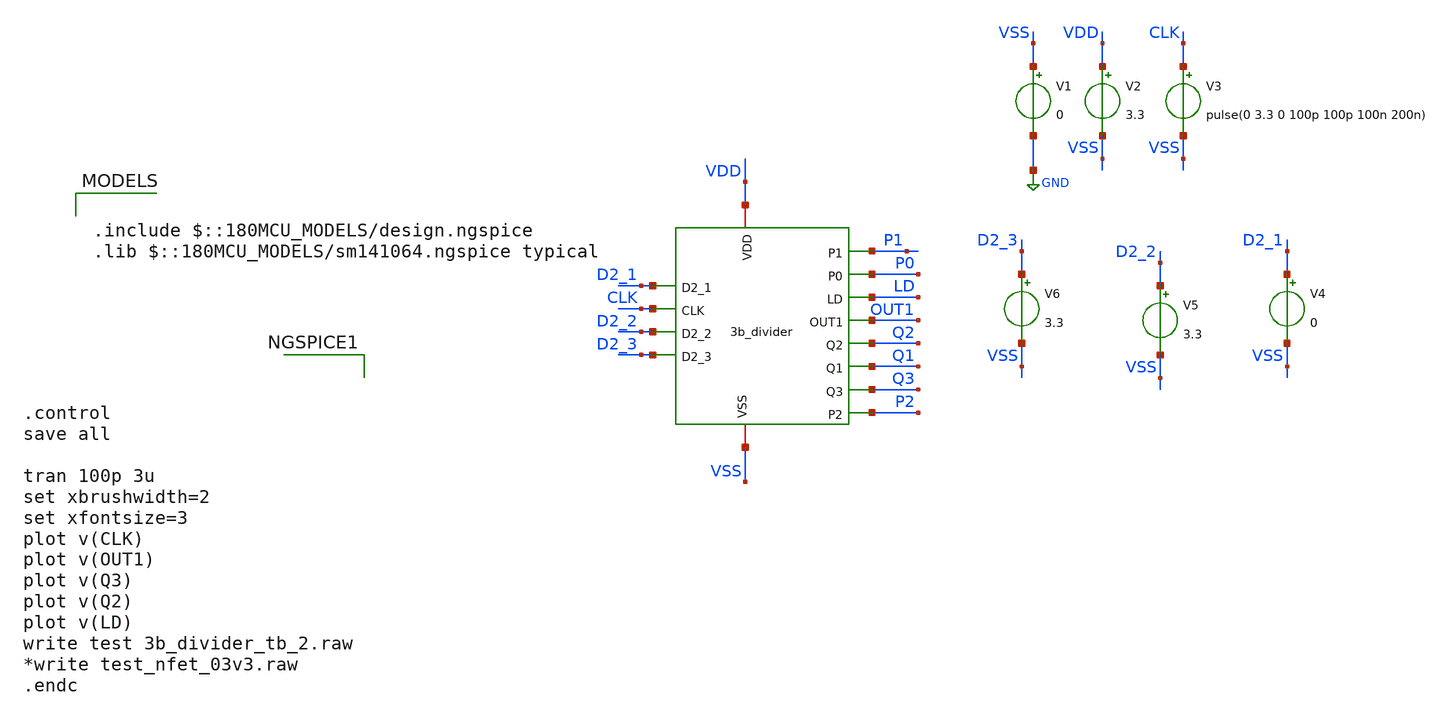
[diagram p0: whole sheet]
** sch_path: Clock_Generator_PAKISTAN_06/Schematics/3b_divider_tb_2.sch
**.subckt 3b_divider_tb_2
x1 VDD P1 P0 D2_1 LD OUT1 CLK Q2 Q1 D2_2 Q3 D2_3 VSS P2 3b_divider
V1 VSS GND 0
V2 VDD VSS 3.3
V3 CLK VSS pulse(0 3.3 0 100p 100p 100n 200n)
V4 D2_1 VSS 0
V5 D2_2 VSS 3.3
V6 D2_3 VSS 3.3
**** begin user architecture code

.include $::180MCU_MODELS/design.ngspice
.lib $::180MCU_MODELS/sm141064.ngspice typical




.control
save all

tran 100p 3u
set xbrushwidth=2
set xfontsize=3
plot v(CLK)
plot v(OUT1)
plot v(Q3)
plot v(Q2)
plot v(LD)
write test 3b_divider_tb_2.raw
*write test_nfet_03v3.raw
.endc


**** end user architecture code
**.ends
.GLOBAL GND
.end
